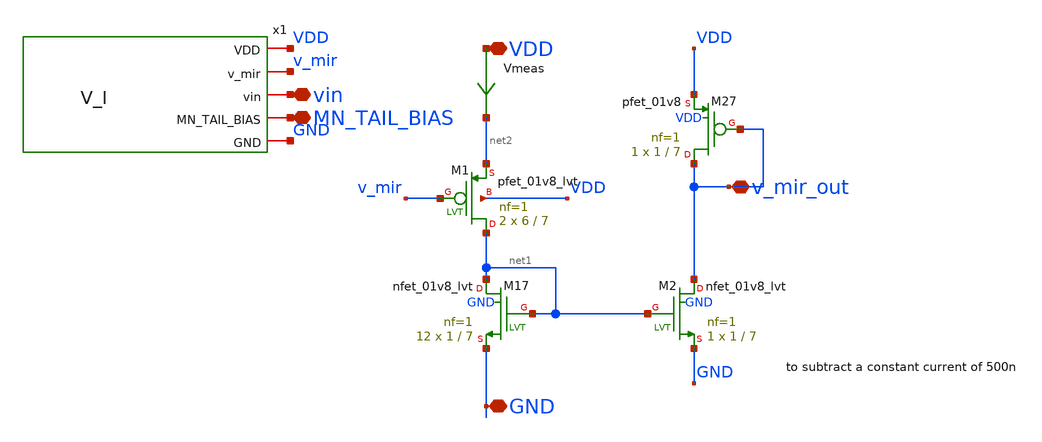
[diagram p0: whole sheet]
** sch_path: xschem/blocks/V_I_complete.sch
**.subckt V_I_complete GND v_mir_out VDD vin MN_TAIL_BIAS
*.iopin GND
*.iopin v_mir_out
*.iopin VDD
*.iopin vin
*.iopin MN_TAIL_BIAS
XM1 net1 v_mir net2 VDD sky130_fd_pr__pfet_01v8_lvt L=7 W=6 nf=1 ad='int((1 + 1)/2) * 6 / 1 * 0.29' as='int((1 + 2)/2) * 6 / 1 * 0.29'
+ pd='2*int((1 + 1)/2) * (6 / 1 + 0.29)' ps='2*int((1 + 2)/2) * (6 / 1 + 0.29)' nrd='0.29 / 6 ' nrs='0.29 / 6 '
+ sa=0 sb=0 sd=0 mult=2 m=2
XM17 net1 net1 GND GND sky130_fd_pr__nfet_01v8_lvt L=7 W=1 nf=1 ad='int((1 + 1)/2) * 1 / 1 * 0.29' as='int((1 + 2)/2) * 1 / 1 * 0.29'
+ pd='2*int((1 + 1)/2) * (1 / 1 + 0.29)' ps='2*int((1 + 2)/2) * (1 / 1 + 0.29)' nrd='0.29 / 1 ' nrs='0.29 / 1 '
+ sa=0 sb=0 sd=0 mult=12 m=12
XM2 v_mir_out net1 GND GND sky130_fd_pr__nfet_01v8_lvt L=7 W=1 nf=1 ad='int((1 + 1)/2) * 1 / 1 * 0.29'
+ as='int((1 + 2)/2) * 1 / 1 * 0.29' pd='2*int((1 + 1)/2) * (1 / 1 + 0.29)' ps='2*int((1 + 2)/2) * (1 / 1 + 0.29)'
+ nrd='0.29 / 1 ' nrs='0.29 / 1 ' sa=0 sb=0 sd=0 mult=1 m=1
XM27 v_mir_out v_mir_out VDD VDD sky130_fd_pr__pfet_01v8 L=7 W=1 nf=1 ad='int((1 + 1)/2) * 1 / 1 * 0.29'
+ as='int((1 + 2)/2) * 1 / 1 * 0.29' pd='2*int((1 + 1)/2) * (1 / 1 + 0.29)' ps='2*int((1 + 2)/2) * (1 / 1 + 0.29)'
+ nrd='0.29 / 1 ' nrs='0.29 / 1 ' sa=0 sb=0 sd=0 mult=1 m=1
x1 VDD v_mir vin MN_TAIL_BIAS GND V_I
Vmeas VDD net2 0
.save i(vmeas)
**.ends
.end
